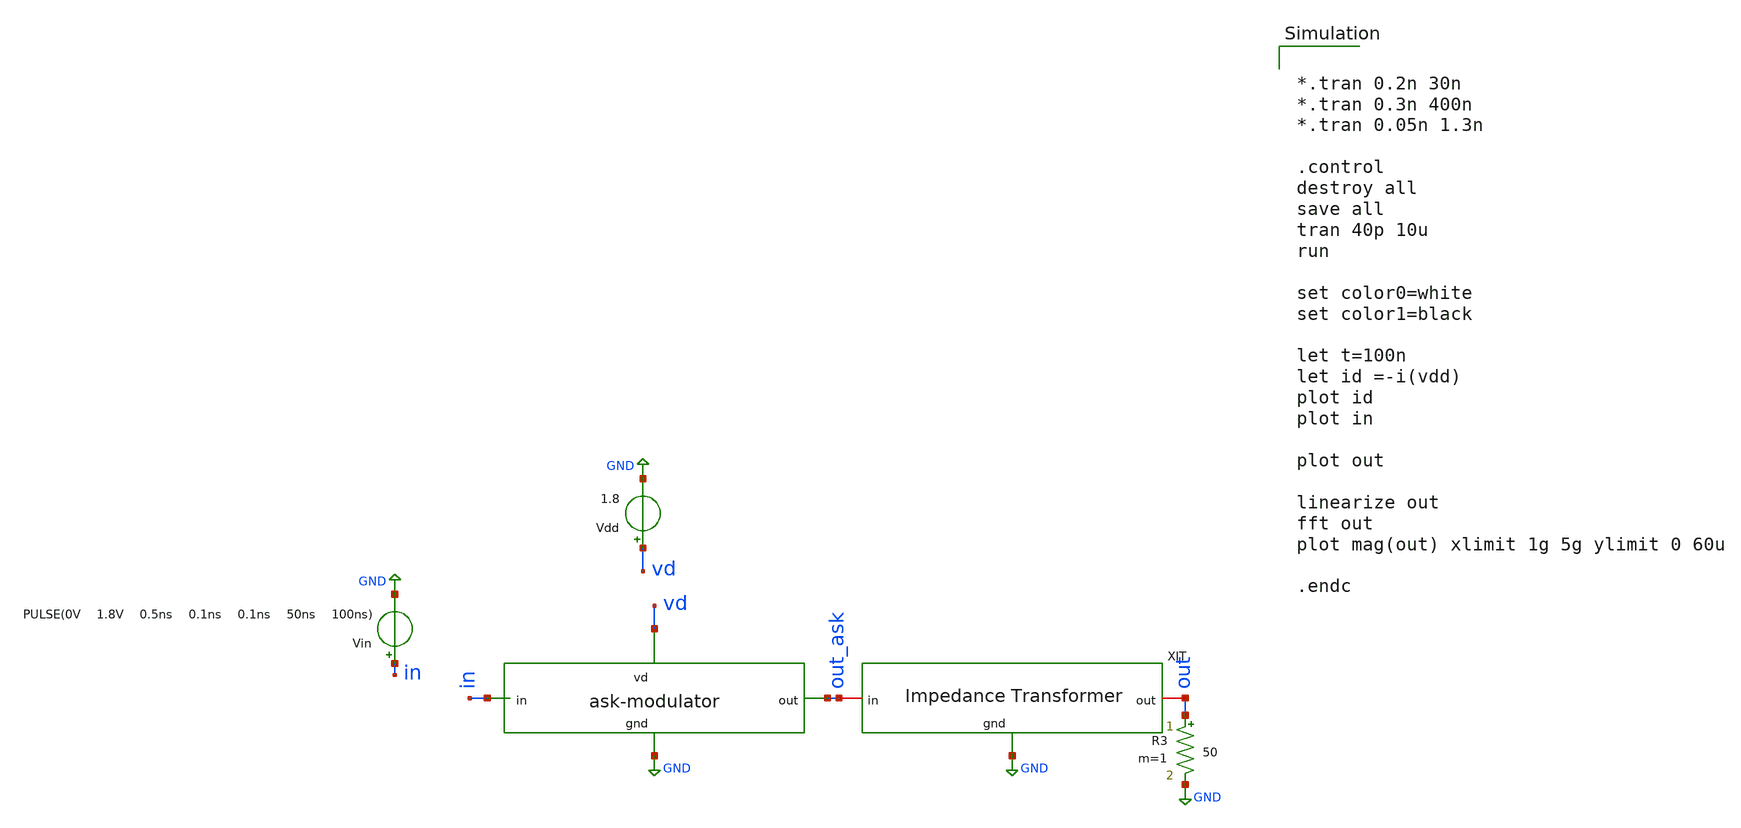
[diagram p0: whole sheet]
** sch_path: impedance-transformer/xschem/impedance-transformer_tb-tran.sch
**.subckt impedance-transformer_tb-tran
Vdd vd GND 1.8
Vin in GND PULSE(0V 1.8V 0.5ns 0.1ns 0.1ns 50ns 100ns)
R3 out GND 50 m=1
x1 out_ask out GND impedance-transformer
x2 vd out_ask in GND ask-modulator
**** begin user architecture code


*.tran 0.2n 30n
*.tran 0.3n 400n
*.tran 0.05n 1.3n

.control
destroy all
save all
tran 40p 10u
run

set color0=white
set color1=black

let t=100n
let id =-i(vdd)
plot id
plot in

plot out

linearize out
fft out
plot mag(out) xlimit 1g 5g ylimit 0 60u

.endc

 .lib $::SKYWATER_MODELS/sky130.lib.spice tt
.include $::SKYWATER_STDCELLS/sky130_fd_sc_hd.spice

**** end user architecture code
**.ends
.GLOBAL GND
.end
